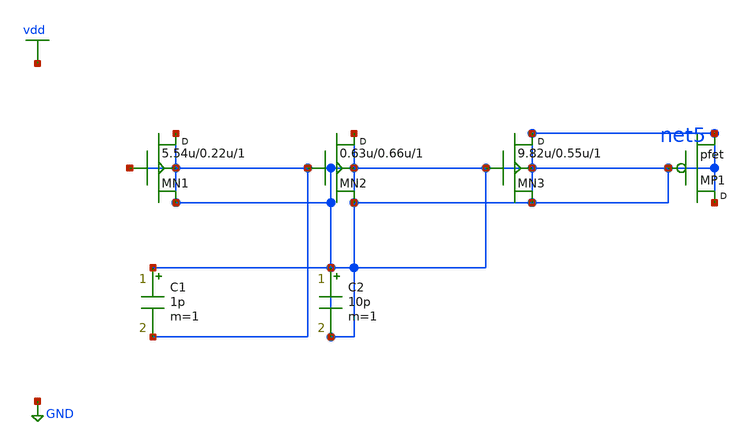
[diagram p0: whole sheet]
** sch_path: synthetic/generated/0023_synthetic.sch
**.subckt 0023_synthetic
MN1 net5 net5 net5 net5 nfet w=5.54u l=0.22u m=1
MN2 net5 net5 net5 net5 nfet w=0.63u l=0.66u m=1
MN3 net5 net5 net5 net5 nfet w=9.82u l=0.55u m=1
MP1 net5 net5 net5 pfet m=1
C1 net5 net5 1p m=1
C2 net5 net5 10p m=1
**.ends
.GLOBAL vdd
.GLOBAL GND
.end
